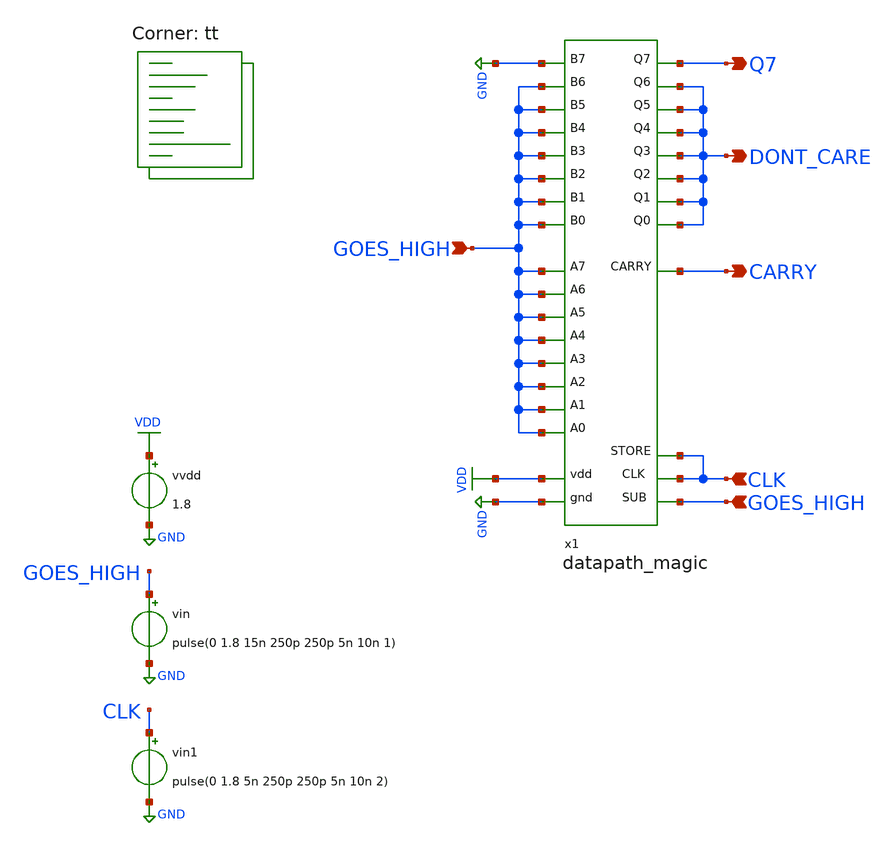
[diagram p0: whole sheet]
** sch_path: xschem/testbench_magic.sch
**.subckt testbench_magic GOES_HIGH GOES_HIGH DONT_CARE Q7 CARRY CLK
*.ipin GOES_HIGH
*.ipin GOES_HIGH
*.opin DONT_CARE
*.opin Q7
*.opin CARRY
*.ipin CLK
x1 GND VDD GOES_HIGH GOES_HIGH GOES_HIGH GOES_HIGH GOES_HIGH GOES_HIGH GOES_HIGH GOES_HIGH GOES_HIGH
+ GOES_HIGH GOES_HIGH GOES_HIGH GOES_HIGH GOES_HIGH GOES_HIGH GND GOES_HIGH CLK CLK DONT_CARE DONT_CARE
+ DONT_CARE DONT_CARE DONT_CARE DONT_CARE DONT_CARE Q7 CARRY datapath_magic
vvdd VDD GND 1.8
vin GOES_HIGH GND pulse(0 1.8 15n 250p 250p 5n 10n 1)
vin1 CLK GND pulse(0 1.8 5n 250p 250p 5n 10n 2)
**** begin user architecture code
.lib $::SKYWATER_MODELS/sky130.lib.spice tt


.control
TRAN 5p 20n
save all
set filetype=binary
write testbench_magic.raw v(CLK) v(GOES_HIGH) v(Q7) v(CARRY)
.endc


**** end user architecture code
**.ends

* expanding   symbol:  datapath_magic.sym # of pins=30
** sym_path: xschem/datapath_magic.sym
.include datapath_magic.spice
.GLOBAL GND
.GLOBAL VDD
.end
